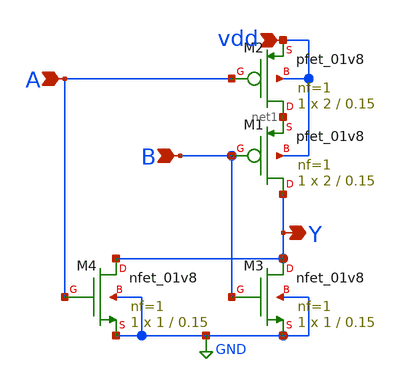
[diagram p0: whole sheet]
** sch_path: Circuit Files/Logic gate design using MOSFETS/gates/NOT_GATE.sch
**.subckt NOT_GATE A B vdd Y
*.ipin A
*.ipin B
*.ipin vdd
*.opin Y
XM1 Y B net1 vdd sky130_fd_pr__pfet_01v8 L=0.15 W=2 nf=1 ad='int((nf+1)/2) * W/nf * 0.29' as='int((nf+2)/2) * W/nf * 0.29'
+ pd='2*int((nf+1)/2) * (W/nf + 0.29)' ps='2*int((nf+2)/2) * (W/nf + 0.29)' nrd='0.29 / W' nrs='0.29 / W'
+ sa=0 sb=0 sd=0 mult=1 m=1
XM2 net1 A vdd vdd sky130_fd_pr__pfet_01v8 L=0.15 W=2 nf=1 ad='int((nf+1)/2) * W/nf * 0.29' as='int((nf+2)/2) * W/nf * 0.29'
+ pd='2*int((nf+1)/2) * (W/nf + 0.29)' ps='2*int((nf+2)/2) * (W/nf + 0.29)' nrd='0.29 / W' nrs='0.29 / W'
+ sa=0 sb=0 sd=0 mult=1 m=1
XM3 Y B GND GND sky130_fd_pr__nfet_01v8 L=0.15 W=1 nf=1 ad='int((nf+1)/2) * W/nf * 0.29' as='int((nf+2)/2) * W/nf * 0.29'
+ pd='2*int((nf+1)/2) * (W/nf + 0.29)' ps='2*int((nf+2)/2) * (W/nf + 0.29)' nrd='0.29 / W' nrs='0.29 / W'
+ sa=0 sb=0 sd=0 mult=1 m=1
XM4 Y A GND GND sky130_fd_pr__nfet_01v8 L=0.15 W=1 nf=1 ad='int((nf+1)/2) * W/nf * 0.29' as='int((nf+2)/2) * W/nf * 0.29'
+ pd='2*int((nf+1)/2) * (W/nf + 0.29)' ps='2*int((nf+2)/2) * (W/nf + 0.29)' nrd='0.29 / W' nrs='0.29 / W'
+ sa=0 sb=0 sd=0 mult=1 m=1
**.ends
.GLOBAL GND
.end
